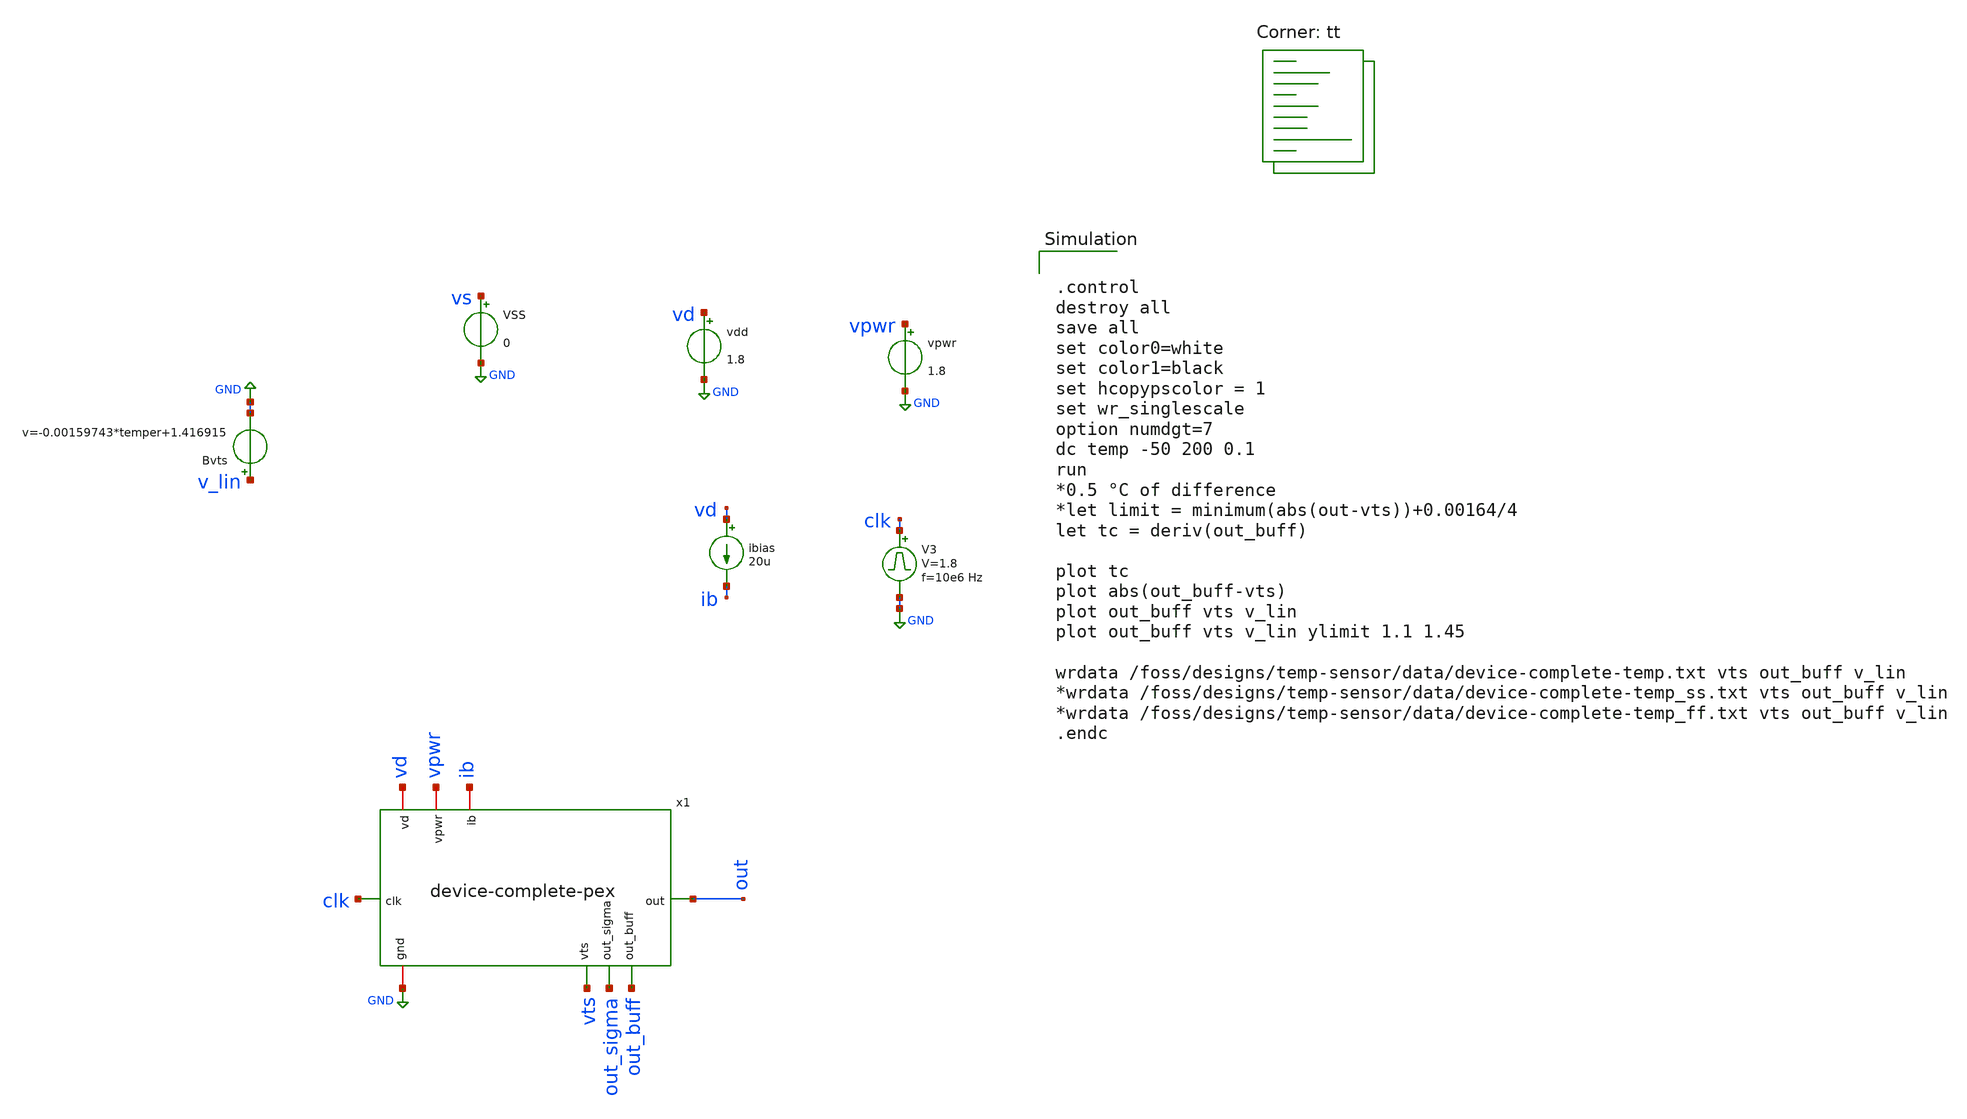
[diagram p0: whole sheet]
** sch_path: device-complete/xschem/device-complete_temp-tb .sch
**.subckt device-complete_temp-tb
Bvts v_lin GND v=-0.00159743*temper+1.416915
vpwr vpwr GND 1.8
V3 clk GND pulse 0 1.8 '0.495/ 10e6 ' '0.01/10e6 ' '0.01/10e6 ' '0.49/10e6 ' '1/10e6 '
vdd vd GND 1.8
ibias vd ib 20u
VSS vs GND 0
x1 vd clk out vpwr ib GND out_buff out_sigma vts device-complete-pex
**** begin user architecture code


.control
destroy all
save all
set color0=white
set color1=black
set hcopypscolor = 1
set wr_singlescale
option numdgt=7
dc temp -50 200 0.1
run
*0.5 °C of difference
*let limit = minimum(abs(out-vts))+0.00164/4
let tc = deriv(out_buff)

plot tc
plot abs(out_buff-vts)
plot out_buff vts v_lin
plot out_buff vts v_lin ylimit 1.1 1.45

wrdata /foss/designs/temp-sensor/data/device-complete-temp.txt vts out_buff v_lin
*wrdata /foss/designs/temp-sensor/data/device-complete-temp_ss.txt vts out_buff v_lin
*wrdata /foss/designs/temp-sensor/data/device-complete-temp_ff.txt vts out_buff v_lin
.endc


.lib $::SKYWATER_MODELS/sky130.lib.spice tt
**** end user architecture code
**.ends
.GLOBAL GND
.end
